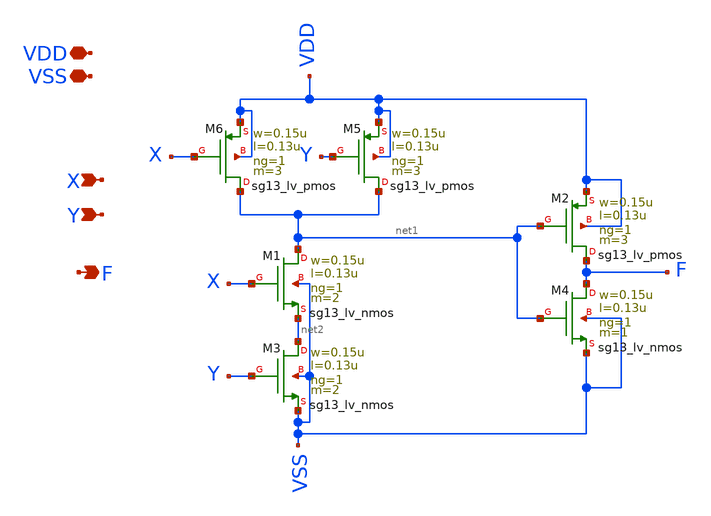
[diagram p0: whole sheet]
** sch_path: xschem/DigitalGates/AND.sch
**.subckt AND VDD X F VSS Y
*.iopin VDD
*.ipin X
*.opin F
*.iopin VSS
*.ipin Y
XM1 net1 X net2 VSS sg13_lv_nmos w=0.15u l=0.13u ng=1 m=2 mm_ok=1
XM2 F net1 VDD VDD sg13_lv_pmos w=0.15u l=0.13u ng=1 m=3 mm_ok=1
XM4 F net1 VSS VSS sg13_lv_nmos w=0.15u l=0.13u ng=1 m=1 mm_ok=1
XM5 net1 Y VDD VDD sg13_lv_pmos w=0.15u l=0.13u ng=1 m=3 mm_ok=1
XM6 net1 X VDD VDD sg13_lv_pmos w=0.15u l=0.13u ng=1 m=3 mm_ok=1
XM3 net2 Y VSS VSS sg13_lv_nmos w=0.15u l=0.13u ng=1 m=2 mm_ok=1
**** begin user architecture code



**** end user architecture code
**.ends
.end
